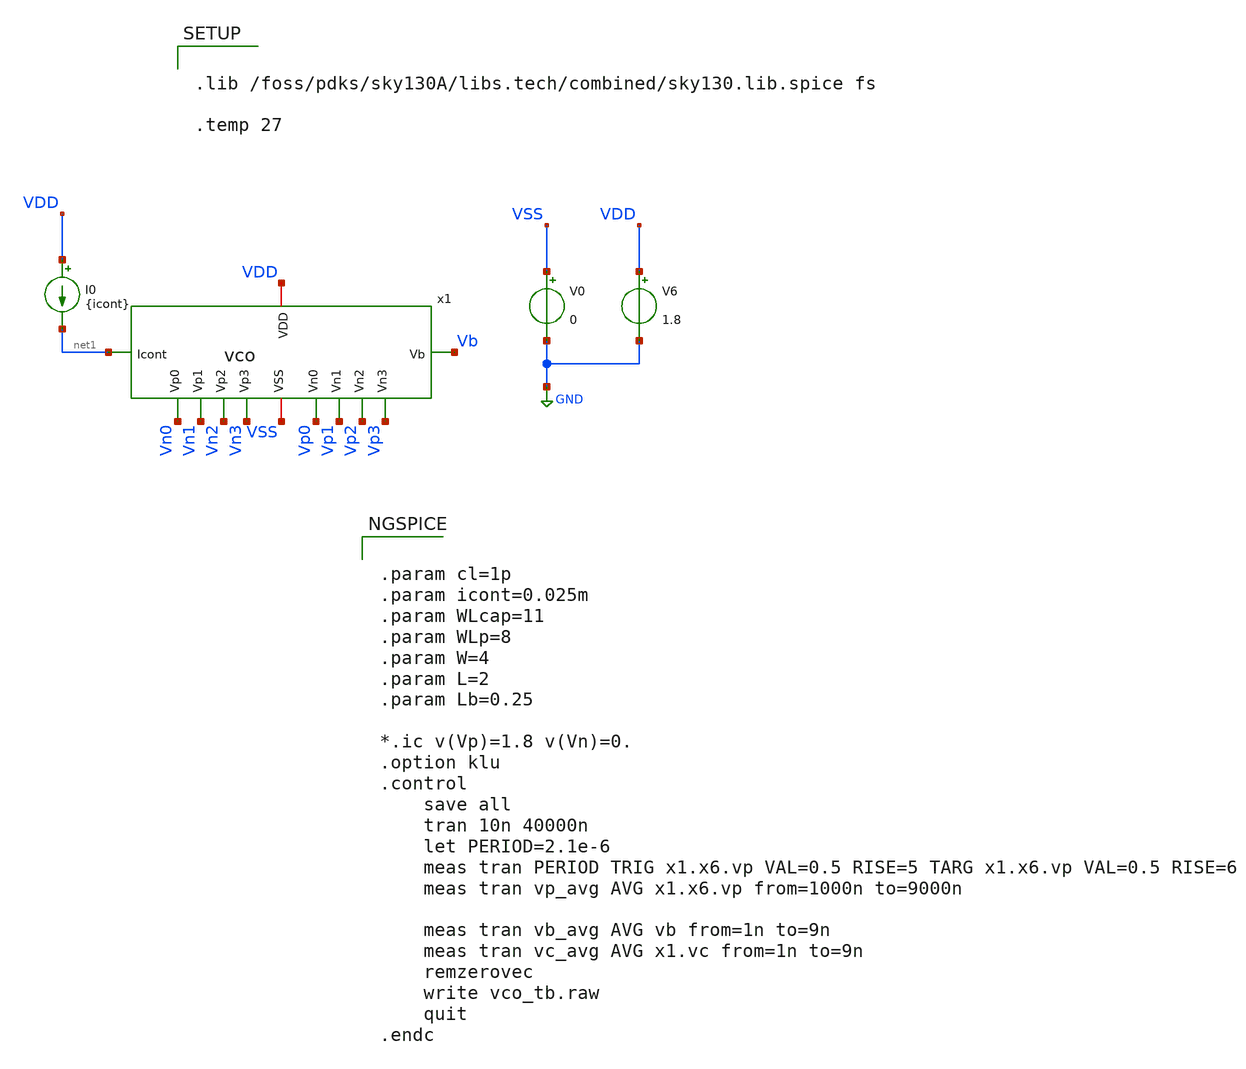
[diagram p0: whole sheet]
** sch_path: xschem/vco_tb.sch
**.subckt vco_tb
V0 VSS GND 0
V6 VDD GND 1.8
I0 VDD net1 {icont}
x1 VDD VSS net1 Vn0 Vn1 Vn2 Vn3 Vp0 Vp1 Vp2 Vp3 Vb vco
**** begin user architecture code


.param cl=1p
.param icont=0.025m
.param WLcap=11
.param WLp=8
.param W=4
.param L=2
.param Lb=0.25

*.ic v(Vp)=1.8 v(Vn)=0.
.option klu
.control
	save all
	tran 10n 40000n
	let PERIOD=2.1e-6
	meas tran PERIOD TRIG x1.x6.vp VAL=0.5 RISE=5 TARG x1.x6.vp VAL=0.5 RISE=6
	meas tran vp_avg AVG x1.x6.vp from=1000n to=9000n

	meas tran vb_avg AVG vb from=1n to=9n
	meas tran vc_avg AVG x1.vc from=1n to=9n
	remzerovec
	write vco_tb.raw
	quit
.endc




.lib /foss/pdks/sky130A/libs.tech/combined/sky130.lib.spice fs

.temp 27


**** end user architecture code
**.ends

* expanding   symbol:  vco.sym # of pins=12
** sym_path: xschem-pex/vco.sym
.include ./vco.spice
.GLOBAL GND
.end
